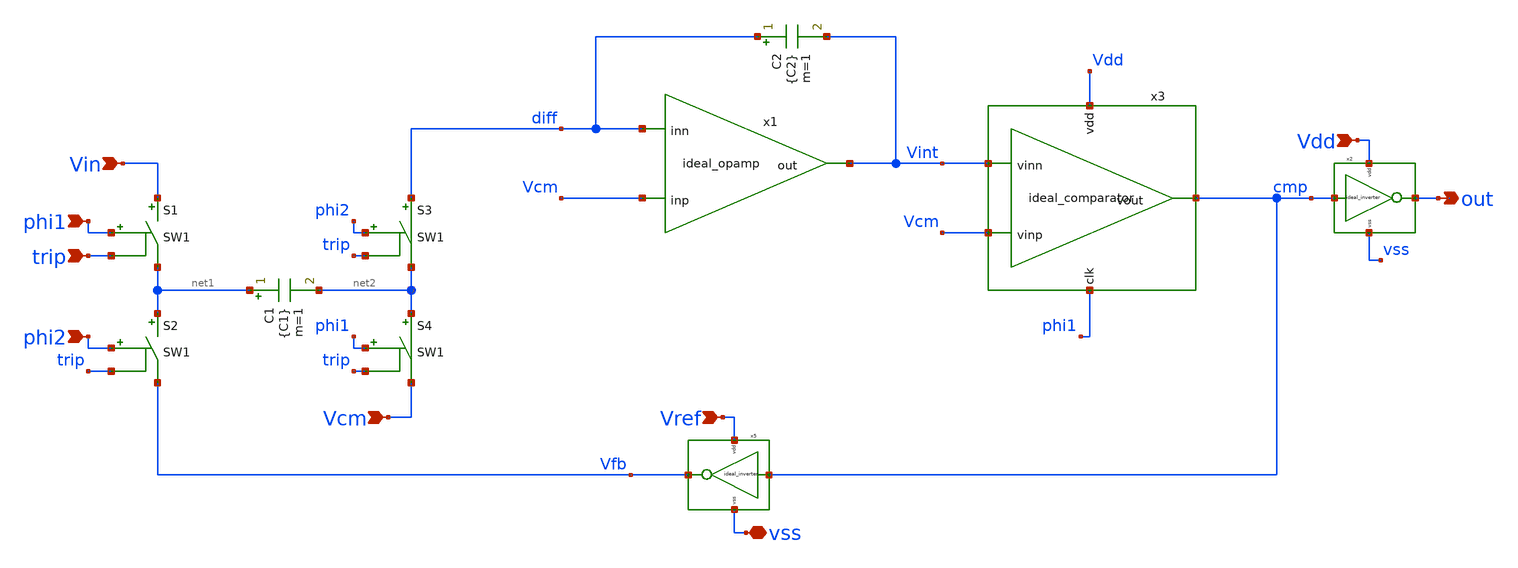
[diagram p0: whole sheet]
** sch_path: 2_ideal_circuits/ideal_modulator.sch
**.subckt ideal_modulator out Vin phi1 trip phi2 Vcm Vref Vdd vss
*.opin out
*.ipin Vin
*.ipin phi1
*.ipin trip
*.ipin phi2
*.ipin Vcm
*.ipin Vref
*.ipin Vdd
*.iopin vss
S1 Vin net1 phi1 trip SW1
S2 net1 Vfb phi2 trip SW1
S3 diff net2 phi2 trip SW1
S4 net2 Vcm phi1 trip SW1
x1 Vcm diff Vint ideal_opamp
C2 diff Vint {C2} m=1
C1 net1 net2 {C1} m=1
x3 Vdd cmp Vint Vcm phi1 ideal_comparator
x5 Vfb cmp vss Vref ideal_inverter
x2 out cmp vss Vdd ideal_inverter
**.ends

* expanding   symbol:  ideal_opamp.sym # of pins=3
** sym_path: ideal_opamp.sym
** sch_path: ideal_opamp.sch
.subckt ideal_opamp inp inn out
*.opin out
*.ipin inp
*.ipin inn
E1 out GND inp inn 1Meg
R1 out GND 100Meg m=1
.ends


* expanding   symbol:  ideal_comparator.sym # of pins=5
** sym_path: 2_ideal_circuits/ideal_comparator.sym
** sch_path: 2_ideal_circuits/ideal_comparator.sch
.subckt ideal_comparator Vdd Vout Vinn Vinp clk
*.ipin Vinp
*.ipin Vinn
*.opin Vout
*.iopin Vdd
*.iopin clk
E1 diff GND Vinp Vinn 1
S1 diff sample tp clk SW1
E2 net1 GND sample GND 1
C1 sample GND 100p m=1
S2 net1 hold clk tp SW1
C2 hold GND 100p m=1
B1 Vout GND V={v(hold)>0?v(Vdd):0}
Etp tp GND Vdd GND 0.5
**** begin user architecture code


.ic v(hold)=1 v(sample)=1


**** end user architecture code
.ends


* expanding   symbol:  ideal_inverter.sym # of pins=4
** sym_path: 2_ideal_circuits/ideal_inverter.sym
** sch_path: 2_ideal_circuits/ideal_inverter.sch
.subckt ideal_inverter out in vss vdd
*.iopin vdd
*.ipin in
*.opin out
*.iopin vss
B1 out GND V={v(in)>v(vdd)/2?v(vss):v(vdd)}
* noconn vdd
* noconn in
* noconn vss
.ends

.GLOBAL GND
**** begin user architecture code
.MODEL SW1 SW( VT=0.9 VH=0.01 RON=0.01 ROFF=10G )
**** end user architecture code
.end
